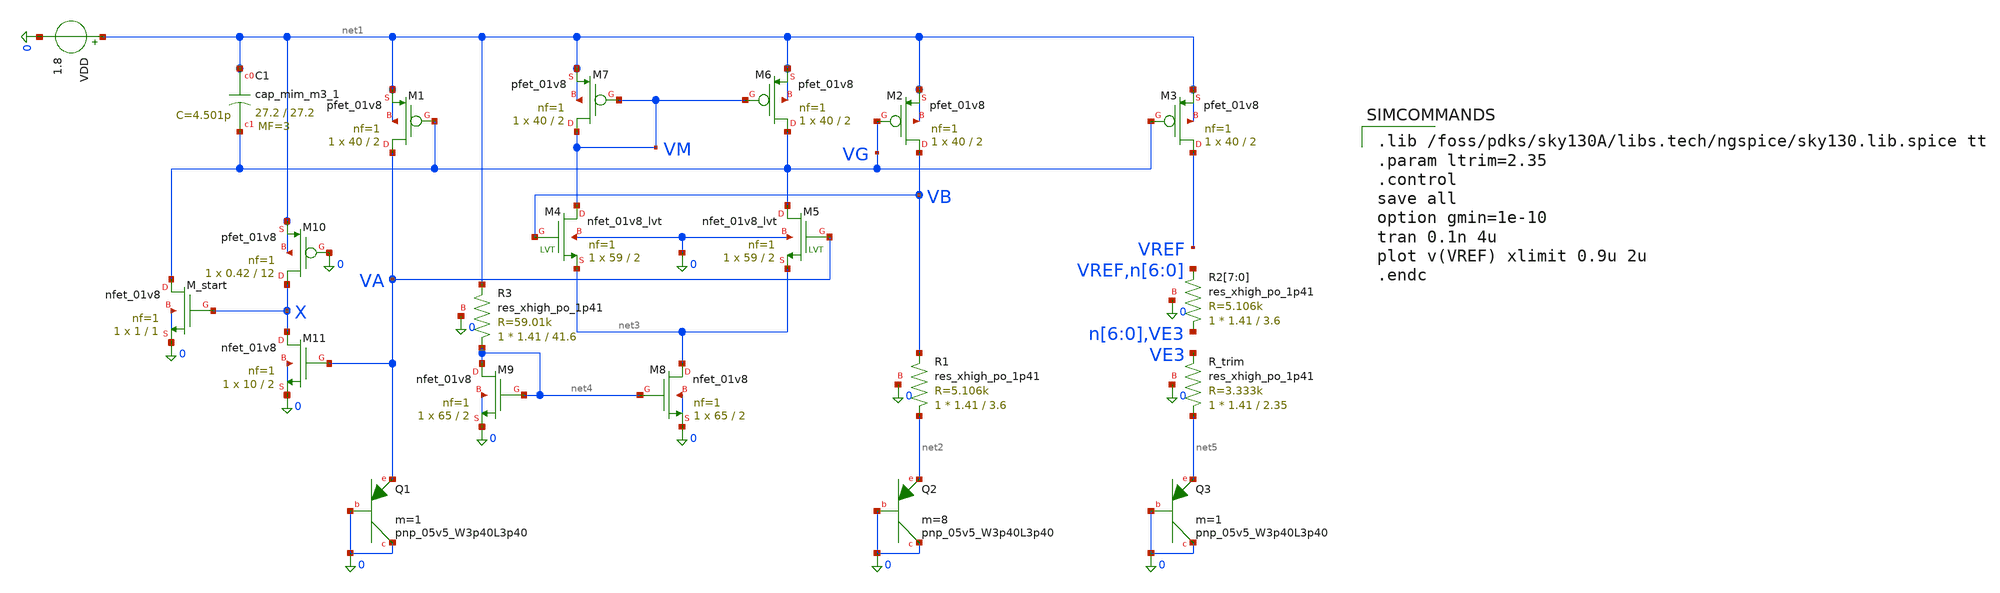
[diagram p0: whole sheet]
** sch_path: bandgap.sch
**.subckt bandgap
XM1 VA VG net1 net1 sky130_fd_pr__pfet_01v8 L=2 W=40 nf=1 ad='int((1 + 1)/2) * 40 / 1 * 0.29' as='int((1 + 2)/2) * 40 / 1 * 0.29'
+ pd='2*int((1 + 1)/2) * (40 / 1 + 0.29)' ps='2*int((1 + 2)/2) * (40 / 1 + 0.29)' nrd='0.29 / 40 ' nrs='0.29 / 40 '
+ sa=0 sb=0 sd=0 mult=1 m=1
XM2 VB VG net1 net1 sky130_fd_pr__pfet_01v8 L=2 W=40 nf=1 ad='int((1 + 1)/2) * 40 / 1 * 0.29' as='int((1 + 2)/2) * 40 / 1 * 0.29'
+ pd='2*int((1 + 1)/2) * (40 / 1 + 0.29)' ps='2*int((1 + 2)/2) * (40 / 1 + 0.29)' nrd='0.29 / 40 ' nrs='0.29 / 40 '
+ sa=0 sb=0 sd=0 mult=1 m=1
XM3 VREF VG net1 net1 sky130_fd_pr__pfet_01v8 L=2 W=40 nf=1 ad='int((1 + 1)/2) * 40 / 1 * 0.29' as='int((1 + 2)/2) * 40 / 1 * 0.29'
+ pd='2*int((1 + 1)/2) * (40 / 1 + 0.29)' ps='2*int((1 + 2)/2) * (40 / 1 + 0.29)' nrd='0.29 / 40 ' nrs='0.29 / 40 '
+ sa=0 sb=0 sd=0 mult=1 m=1
XQ1 0 0 VA sky130_fd_pr__pnp_05v5_W3p40L3p40 m=1
XQ2 0 0 net2 sky130_fd_pr__pnp_05v5_W3p40L3p40 m=8
XQ3 0 0 net5 sky130_fd_pr__pnp_05v5_W3p40L3p40 m=1
VDD net1 0 1.8
XM4 VM VB net3 0 sky130_fd_pr__nfet_01v8_lvt L=2 W=59 nf=1 ad='int((1 + 1)/2) * 59 / 1 * 0.29' as='int((1 + 2)/2) * 59 / 1 * 0.29'
+ pd='2*int((1 + 1)/2) * (59 / 1 + 0.29)' ps='2*int((1 + 2)/2) * (59 / 1 + 0.29)' nrd='0.29 / 59 ' nrs='0.29 / 59 '
+ sa=0 sb=0 sd=0 mult=1 m=1
XM5 VG VA net3 0 sky130_fd_pr__nfet_01v8_lvt L=2 W=59 nf=1 ad='int((1 + 1)/2) * 59 / 1 * 0.29' as='int((1 + 2)/2) * 59 / 1 * 0.29'
+ pd='2*int((1 + 1)/2) * (59 / 1 + 0.29)' ps='2*int((1 + 2)/2) * (59 / 1 + 0.29)' nrd='0.29 / 59 ' nrs='0.29 / 59 '
+ sa=0 sb=0 sd=0 mult=1 m=1
XM6 VG VM net1 net1 sky130_fd_pr__pfet_01v8 L=2 W=40 nf=1 ad='int((1 + 1)/2) * 40 / 1 * 0.29' as='int((1 + 2)/2) * 40 / 1 * 0.29'
+ pd='2*int((1 + 1)/2) * (40 / 1 + 0.29)' ps='2*int((1 + 2)/2) * (40 / 1 + 0.29)' nrd='0.29 / 40 ' nrs='0.29 / 40 '
+ sa=0 sb=0 sd=0 mult=1 m=1
XM7 VM VM net1 net1 sky130_fd_pr__pfet_01v8 L=2 W=40 nf=1 ad='int((1 + 1)/2) * 40 / 1 * 0.29' as='int((1 + 2)/2) * 40 / 1 * 0.29'
+ pd='2*int((1 + 1)/2) * (40 / 1 + 0.29)' ps='2*int((1 + 2)/2) * (40 / 1 + 0.29)' nrd='0.29 / 40 ' nrs='0.29 / 40 '
+ sa=0 sb=0 sd=0 mult=1 m=1
XM8 net3 net4 0 0 sky130_fd_pr__nfet_01v8 L=2 W=65 nf=1 ad='int((1 + 1)/2) * 65 / 1 * 0.29' as='int((1 + 2)/2) * 65 / 1 * 0.29'
+ pd='2*int((1 + 1)/2) * (65 / 1 + 0.29)' ps='2*int((1 + 2)/2) * (65 / 1 + 0.29)' nrd='0.29 / 65 ' nrs='0.29 / 65 '
+ sa=0 sb=0 sd=0 mult=1 m=1
XM9 net4 net4 0 0 sky130_fd_pr__nfet_01v8 L=2 W=65 nf=1 ad='int((1 + 1)/2) * 65 / 1 * 0.29' as='int((1 + 2)/2) * 65 / 1 * 0.29'
+ pd='2*int((1 + 1)/2) * (65 / 1 + 0.29)' ps='2*int((1 + 2)/2) * (65 / 1 + 0.29)' nrd='0.29 / 65 ' nrs='0.29 / 65 '
+ sa=0 sb=0 sd=0 mult=1 m=1
XM10 X 0 net1 net1 sky130_fd_pr__pfet_01v8 L=12 W=0.42 nf=1 ad='int((1 + 1)/2) * 0.42 / 1 * 0.29' as='int((1 + 2)/2) * 0.42 / 1 * 0.29'
+ pd='2*int((1 + 1)/2) * (0.42 / 1 + 0.29)' ps='2*int((1 + 2)/2) * (0.42 / 1 + 0.29)' nrd='0.29 / 0.42 '
+ nrs='0.29 / 0.42 ' sa=0 sb=0 sd=0 mult=1 m=1
XM11 X VA 0 0 sky130_fd_pr__nfet_01v8 L=2 W=10 nf=1 ad='int((1 + 1)/2) * 10 / 1 * 0.29' as='int((1 + 2)/2) * 10 / 1 * 0.29'
+ pd='2*int((1 + 1)/2) * (10 / 1 + 0.29)' ps='2*int((1 + 2)/2) * (10 / 1 + 0.29)' nrd='0.29 / 10 ' nrs='0.29 / 10 '
+ sa=0 sb=0 sd=0 mult=1 m=1
XM_start VG X 0 0 sky130_fd_pr__nfet_01v8 L=1 W=1 nf=1 ad='int((1 + 1)/2) * 1 / 1 * 0.29' as='int((1 + 2)/2) * 1 / 1 * 0.29'
+ pd='2*int((1 + 1)/2) * (1 / 1 + 0.29)' ps='2*int((1 + 2)/2) * (1 / 1 + 0.29)' nrd='0.29 / 1 ' nrs='0.29 / 1 '
+ sa=0 sb=0 sd=0 mult=1 m=1
XR2[7] n[6] VREF 0 sky130_fd_pr__res_xhigh_po_1p41 L=3.6 mult=1 m=1
XR2[6] n[5] n[6] 0 sky130_fd_pr__res_xhigh_po_1p41 L=3.6 mult=1 m=1
XR2[5] n[4] n[5] 0 sky130_fd_pr__res_xhigh_po_1p41 L=3.6 mult=1 m=1
XR2[4] n[3] n[4] 0 sky130_fd_pr__res_xhigh_po_1p41 L=3.6 mult=1 m=1
XR2[3] n[2] n[3] 0 sky130_fd_pr__res_xhigh_po_1p41 L=3.6 mult=1 m=1
XR2[2] n[1] n[2] 0 sky130_fd_pr__res_xhigh_po_1p41 L=3.6 mult=1 m=1
XR2[1] n[0] n[1] 0 sky130_fd_pr__res_xhigh_po_1p41 L=3.6 mult=1 m=1
XR2[0] VE3 n[0] 0 sky130_fd_pr__res_xhigh_po_1p41 L=3.6 mult=1 m=1
XR1 net2 VB 0 sky130_fd_pr__res_xhigh_po_1p41 L=3.6 mult=1 m=1
XR3 net4 net1 0 sky130_fd_pr__res_xhigh_po_1p41 L=41.6 mult=1 m=1
XR_trim net5 VE3 0 sky130_fd_pr__res_xhigh_po_1p41 L=2.35 mult=1 m=1
XC1 net1 VG sky130_fd_pr__cap_mim_m3_1 W=27.2 L=27.2 MF=3 m=3
**** begin user architecture code

.lib /foss/pdks/sky130A/libs.tech/ngspice/sky130.lib.spice tt
.param ltrim=2.35
.control
save all
option gmin=1e-10
tran 0.1n 4u
plot v(VREF) xlimit 0.9u 2u
.endc

**** end user architecture code
**.ends
.end
